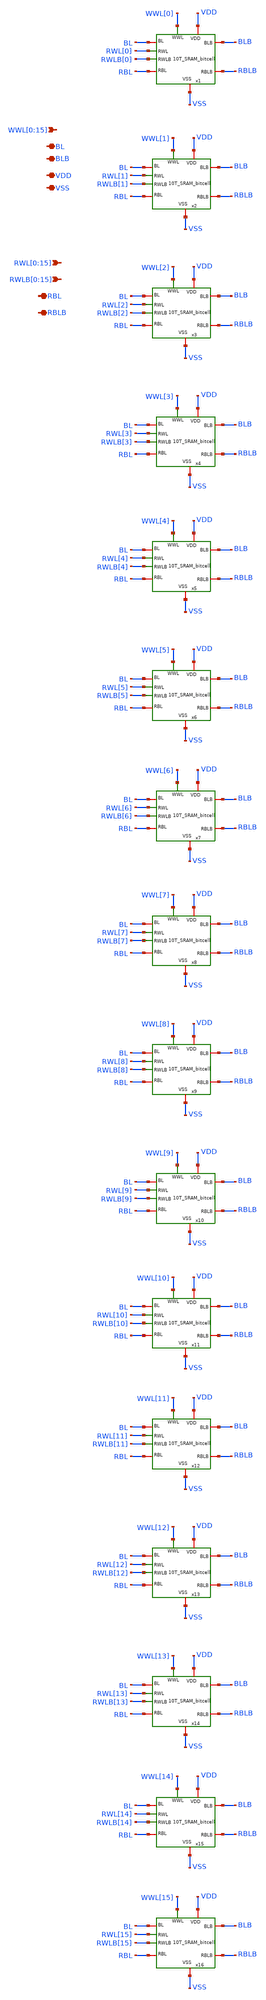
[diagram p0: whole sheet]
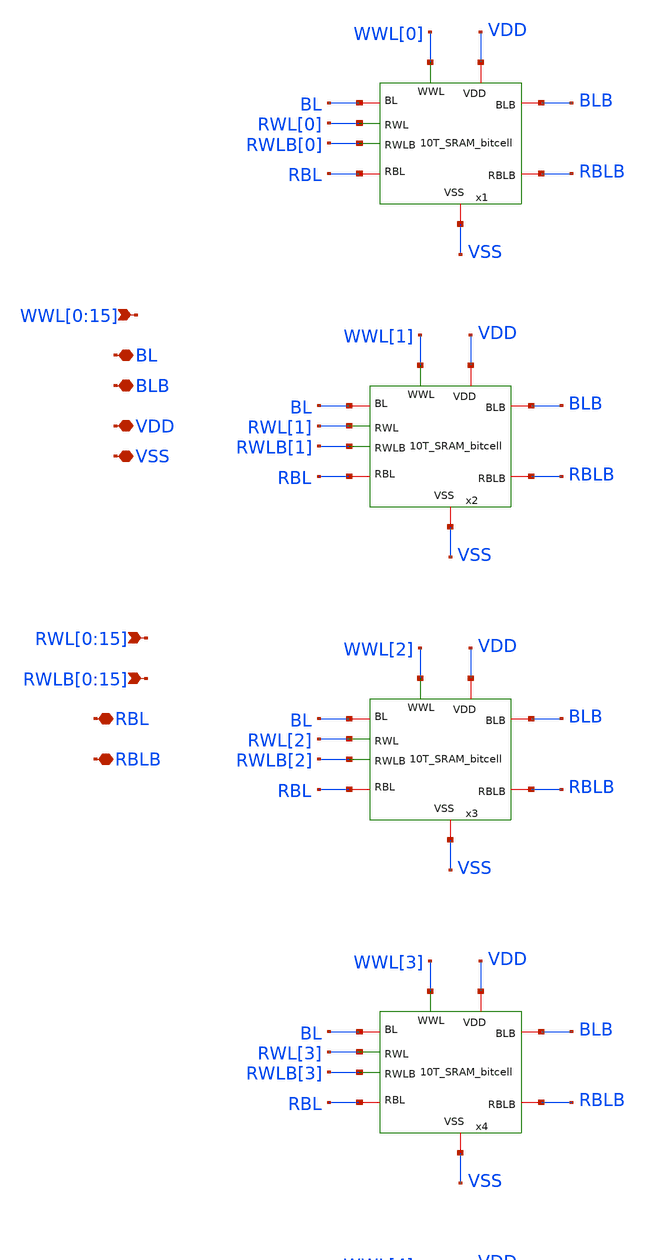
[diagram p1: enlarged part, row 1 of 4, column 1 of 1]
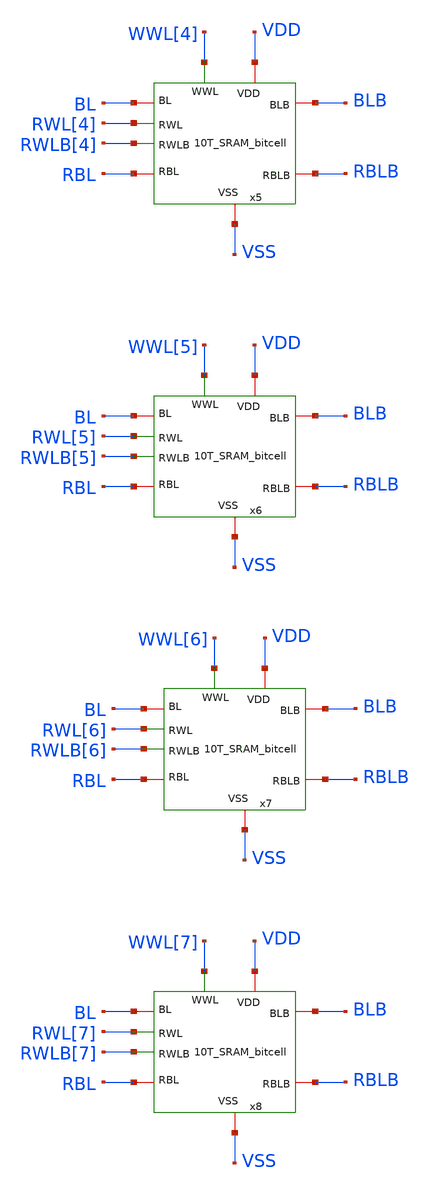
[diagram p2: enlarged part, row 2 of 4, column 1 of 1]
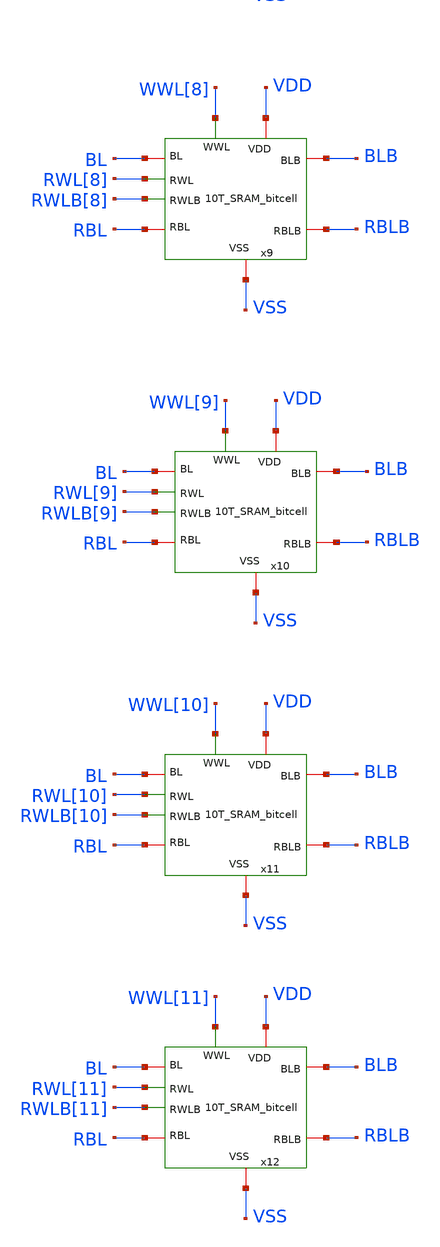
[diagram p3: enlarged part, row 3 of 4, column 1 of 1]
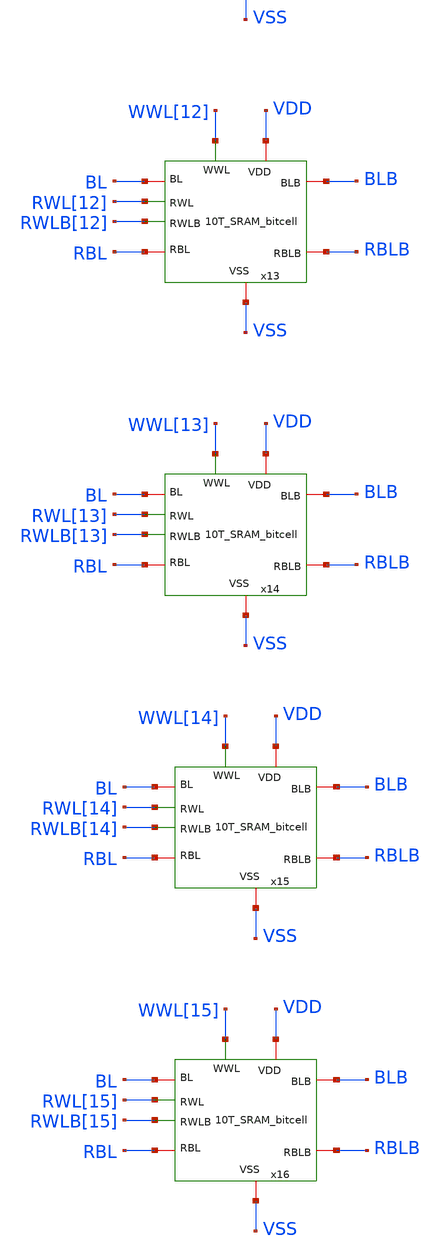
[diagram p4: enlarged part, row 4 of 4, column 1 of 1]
** sch_path: xschem/Integrated_bitcell/10T_SRAM_bitcell_16x1_array.sch
**.subckt 10T_SRAM_bitcell_16x1_array
*+ WWL[0],WWL[1],WWL[2],WWL[3],WWL[4],WWL[5],WWL[6],WWL[7],WWL[8],WWL[9],WWL[10],WWL[11],WWL[12],WWL[13],WWL[14],WWL[15]
*+ RWL[0],RWL[1],RWL[2],RWL[3],RWL[4],RWL[5],RWL[6],RWL[7],RWL[8],RWL[9],RWL[10],RWL[11],RWL[12],RWL[13],RWL[14],RWL[15]
*+ RWLB[0],RWLB[1],RWLB[2],RWLB[3],RWLB[4],RWLB[5],RWLB[6],RWLB[7],RWLB[8],RWLB[9],RWLB[10],RWLB[11],RWLB[12],RWLB[13],RWLB[14],RWLB[15] BL BLB VDD VSS RBL RBLB
*.ipin
*+ WWL[0],WWL[1],WWL[2],WWL[3],WWL[4],WWL[5],WWL[6],WWL[7],WWL[8],WWL[9],WWL[10],WWL[11],WWL[12],WWL[13],WWL[14],WWL[15]
*.ipin
*+ RWL[0],RWL[1],RWL[2],RWL[3],RWL[4],RWL[5],RWL[6],RWL[7],RWL[8],RWL[9],RWL[10],RWL[11],RWL[12],RWL[13],RWL[14],RWL[15]
*.ipin
*+ RWLB[0],RWLB[1],RWLB[2],RWLB[3],RWLB[4],RWLB[5],RWLB[6],RWLB[7],RWLB[8],RWLB[9],RWLB[10],RWLB[11],RWLB[12],RWLB[13],RWLB[14],RWLB[15]
*.iopin BL
*.iopin BLB
*.iopin VDD
*.iopin VSS
*.iopin RBL
*.iopin RBLB
x1 WWL[0] BL BLB VDD VSS RWL[0] RWLB[0] RBL RBLB 10T_SRAM_bitcell
x2 WWL[1] BL BLB VDD VSS RWL[1] RWLB[1] RBL RBLB 10T_SRAM_bitcell
x3 WWL[2] BL BLB VDD VSS RWL[2] RWLB[2] RBL RBLB 10T_SRAM_bitcell
x4 WWL[3] BL BLB VDD VSS RWL[3] RWLB[3] RBL RBLB 10T_SRAM_bitcell
x5 WWL[4] BL BLB VDD VSS RWL[4] RWLB[4] RBL RBLB 10T_SRAM_bitcell
x6 WWL[5] BL BLB VDD VSS RWL[5] RWLB[5] RBL RBLB 10T_SRAM_bitcell
x8 WWL[7] BL BLB VDD VSS RWL[7] RWLB[7] RBL RBLB 10T_SRAM_bitcell
x9 WWL[8] BL BLB VDD VSS RWL[8] RWLB[8] RBL RBLB 10T_SRAM_bitcell
x10 WWL[9] BL BLB VDD VSS RWL[9] RWLB[9] RBL RBLB 10T_SRAM_bitcell
x11 WWL[10] BL BLB VDD VSS RWL[10] RWLB[10] RBL RBLB 10T_SRAM_bitcell
x12 WWL[11] BL BLB VDD VSS RWL[11] RWLB[11] RBL RBLB 10T_SRAM_bitcell
x13 WWL[12] BL BLB VDD VSS RWL[12] RWLB[12] RBL RBLB 10T_SRAM_bitcell
x14 WWL[13] BL BLB VDD VSS RWL[13] RWLB[13] RBL RBLB 10T_SRAM_bitcell
x15 WWL[14] BL BLB VDD VSS RWL[14] RWLB[14] RBL RBLB 10T_SRAM_bitcell
x16 WWL[15] BL BLB VDD VSS RWL[15] RWLB[15] RBL RBLB 10T_SRAM_bitcell
x7 WWL[6] BL BLB VDD VSS RWL[6] RWLB[6] RBL RBLB 10T_SRAM_bitcell
**.ends

* expanding   symbol:  10T_SRAM_bitcell.sym # of pins=9
** sym_path: xschem/Integrated_bitcell/10T_SRAM_bitcell.sym
** sch_path: xschem/Integrated_bitcell/10T_SRAM_bitcell.sch
.subckt 10T_SRAM_bitcell WWL BL BLB VDD VSS RWL RWLB RBL RBLB
*.iopin BL
*.iopin BLB
*.iopin VDD
*.iopin VSS
*.iopin RBL
*.iopin RBLB
*.ipin WWL
*.ipin RWL
*.ipin RWLB
XM1 net1 net2 VSS VSS sky130_fd_pr__nfet_01v8 L=0.15 W=0.64 nf=1 ad='int((nf+1)/2) * W/nf * 0.29' as='int((nf+2)/2) * W/nf * 0.29'
+ pd='2*int((nf+1)/2) * (W/nf + 0.29)' ps='2*int((nf+2)/2) * (W/nf + 0.29)' nrd='0.29 / W' nrs='0.29 / W'
+ sa=0 sb=0 sd=0 mult=1 m=1
XM2 net2 net1 VSS VSS sky130_fd_pr__nfet_01v8 L=0.15 W=0.64 nf=1 ad='int((nf+1)/2) * W/nf * 0.29' as='int((nf+2)/2) * W/nf * 0.29'
+ pd='2*int((nf+1)/2) * (W/nf + 0.29)' ps='2*int((nf+2)/2) * (W/nf + 0.29)' nrd='0.29 / W' nrs='0.29 / W'
+ sa=0 sb=0 sd=0 mult=1 m=1
XM3 net2 net1 VDD VDD sky130_fd_pr__pfet_01v8 L=0.15 W=0.42 nf=1 ad='int((nf+1)/2) * W/nf * 0.29' as='int((nf+2)/2) * W/nf * 0.29'
+ pd='2*int((nf+1)/2) * (W/nf + 0.29)' ps='2*int((nf+2)/2) * (W/nf + 0.29)' nrd='0.29 / W' nrs='0.29 / W'
+ sa=0 sb=0 sd=0 mult=1 m=1
XM4 net1 net2 VDD VDD sky130_fd_pr__pfet_01v8 L=0.15 W=0.42 nf=1 ad='int((nf+1)/2) * W/nf * 0.29' as='int((nf+2)/2) * W/nf * 0.29'
+ pd='2*int((nf+1)/2) * (W/nf + 0.29)' ps='2*int((nf+2)/2) * (W/nf + 0.29)' nrd='0.29 / W' nrs='0.29 / W'
+ sa=0 sb=0 sd=0 mult=1 m=1
XM6 net1 WWL BLB VSS sky130_fd_pr__nfet_01v8 L=0.15 W=0.42 nf=1 ad='int((nf+1)/2) * W/nf * 0.29' as='int((nf+2)/2) * W/nf * 0.29'
+ pd='2*int((nf+1)/2) * (W/nf + 0.29)' ps='2*int((nf+2)/2) * (W/nf + 0.29)' nrd='0.29 / W' nrs='0.29 / W'
+ sa=0 sb=0 sd=0 mult=1 m=1
XM5 net2 WWL BL VSS sky130_fd_pr__nfet_01v8 L=0.15 W=0.42 nf=1 ad='int((nf+1)/2) * W/nf * 0.29' as='int((nf+2)/2) * W/nf * 0.29'
+ pd='2*int((nf+1)/2) * (W/nf + 0.29)' ps='2*int((nf+2)/2) * (W/nf + 0.29)' nrd='0.29 / W' nrs='0.29 / W'
+ sa=0 sb=0 sd=0 mult=1 m=1
XM7 VSS net2 net3 VSS sky130_fd_pr__nfet_01v8 L=0.15 W=0.42 nf=1 ad='int((nf+1)/2) * W/nf * 0.29' as='int((nf+2)/2) * W/nf * 0.29'
+ pd='2*int((nf+1)/2) * (W/nf + 0.29)' ps='2*int((nf+2)/2) * (W/nf + 0.29)' nrd='0.29 / W' nrs='0.29 / W'
+ sa=0 sb=0 sd=0 mult=1 m=1
XM8 RBL RWL net3 VSS sky130_fd_pr__nfet_01v8 L=0.15 W=0.42 nf=1 ad='int((nf+1)/2) * W/nf * 0.29' as='int((nf+2)/2) * W/nf * 0.29'
+ pd='2*int((nf+1)/2) * (W/nf + 0.29)' ps='2*int((nf+2)/2) * (W/nf + 0.29)' nrd='0.29 / W' nrs='0.29 / W'
+ sa=0 sb=0 sd=0 mult=1 m=1
XM9 VSS net1 net4 VSS sky130_fd_pr__nfet_01v8 L=0.15 W=0.42 nf=1 ad='int((nf+1)/2) * W/nf * 0.29' as='int((nf+2)/2) * W/nf * 0.29'
+ pd='2*int((nf+1)/2) * (W/nf + 0.29)' ps='2*int((nf+2)/2) * (W/nf + 0.29)' nrd='0.29 / W' nrs='0.29 / W'
+ sa=0 sb=0 sd=0 mult=1 m=1
XM10 RBLB RWLB net4 VSS sky130_fd_pr__nfet_01v8 L=0.15 W=0.42 nf=1 ad='int((nf+1)/2) * W/nf * 0.29' as='int((nf+2)/2) * W/nf * 0.29'
+ pd='2*int((nf+1)/2) * (W/nf + 0.29)' ps='2*int((nf+2)/2) * (W/nf + 0.29)' nrd='0.29 / W' nrs='0.29 / W'
+ sa=0 sb=0 sd=0 mult=1 m=1
.ends

.end
